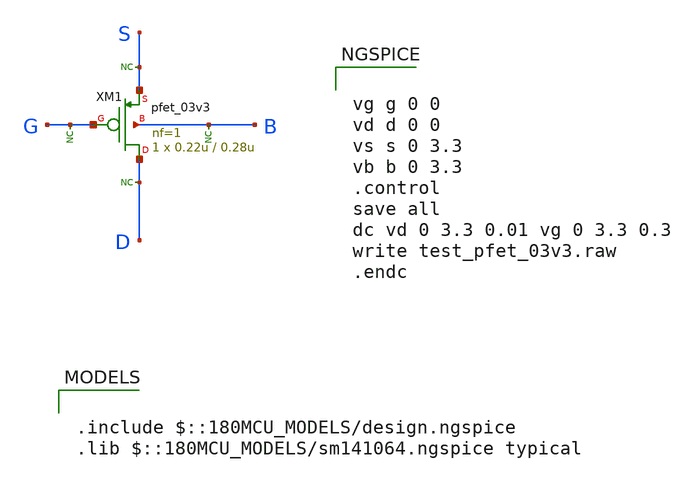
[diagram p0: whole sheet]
** sch_path: cells/xschem/tests/test_pfet_03v3.sch
* Copyright 2022 GlobalFoundries PDK Authors
* Licensed under the Apache License, Version 2.0 (the "License");
* you may not use this file except in compliance with the License.
* You may obtain a copy of the License at
* https://www.apache.org/licenses/LICENSE-2.0
* Unless required by applicable law or agreed to in writing, software
* distributed under the License is distributed on an "AS IS" BASIS,
* WITHOUT WARRANTIES OR CONDITIONS OF ANY KIND, either express or implied.
* See the License for the specific language governing permissions and
* limitations under the License.
**.subckt test_pfet_03v3
XM1 D G S B pfet_03v3 L=0.28u W=0.22u nf=1 ad='int((nf+1)/2) * W/nf * 0.18u' as='int((nf+2)/2) * W/nf * 0.18u'
+ pd='2*int((nf+1)/2) * (W/nf + 0.18u)' ps='2*int((nf+2)/2) * (W/nf + 0.18u)' nrd='0.18u / W' nrs='0.18u / W'
+ sa=0 sb=0 sd=0 m=1
* noconn S
* noconn D
* noconn G
* noconn B
**** begin user architecture code


vg g 0 0
vd d 0 0
vs s 0 3.3
vb b 0 3.3
.control
save all
dc vd 0 3.3 0.01 vg 0 3.3 0.3
write test_pfet_03v3.raw
.endc



.include $::180MCU_MODELS/design.ngspice
.lib $::180MCU_MODELS/sm141064.ngspice typical

**** end user architecture code
**.ends
.end
